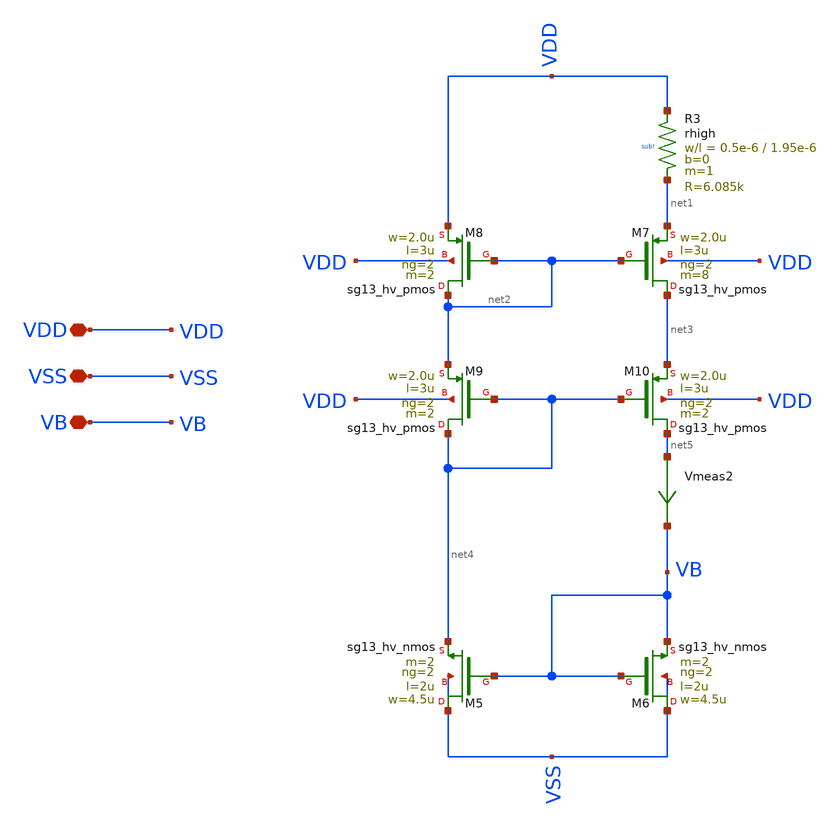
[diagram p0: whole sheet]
** sch_path: my_ip/LIB/ihp-sg13g2/FD_opamp001/bias_cell.sch
**.subckt bias_cell VDD VSS VB
*.iopin VDD
*.iopin VSS
*.iopin VB
XM5 VSS VB net4 VSS sg13_hv_nmos w=4.5u l=2u ng=2 m=2 mm_ok=1
XM6 VSS VB VB VSS sg13_hv_nmos w=4.5u l=2u ng=2 m=2 mm_ok=1
XR3 VDD net1 sub! rhigh w=0.5e-6 l=1.95e-6 m=1 b=0 mm_ok=1
XM7 net3 net2 net1 VDD sg13_hv_pmos w=2.0u l=3u ng=2 m=8 mm_ok=1
XM8 net2 net2 VDD VDD sg13_hv_pmos w=2.0u l=3u ng=2 m=2 mm_ok=1
XM9 net4 net4 net2 VDD sg13_hv_pmos w=2.0u l=3u ng=2 m=2 mm_ok=1
XM10 net5 net4 net3 VDD sg13_hv_pmos w=2.0u l=3u ng=2 m=2 mm_ok=1
Vmeas2 net5 VB 0
.save i(vmeas2)
**.ends
.end
